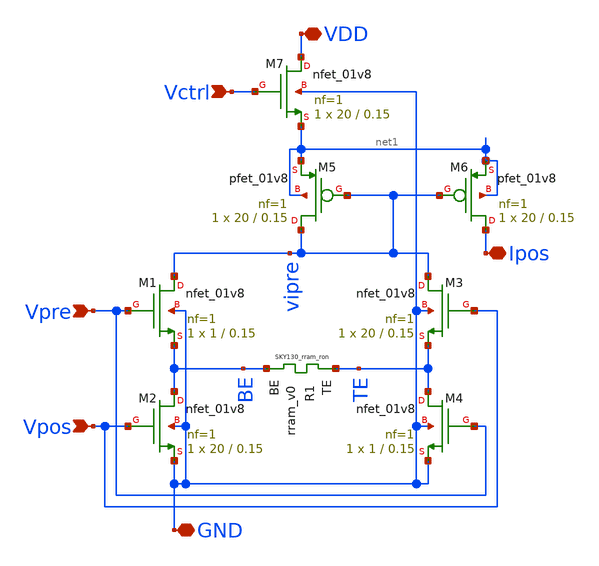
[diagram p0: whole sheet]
** sch_path: synapse/7T1R.sch
**.subckt 7T1R Vpre Vpos GND Ipos VDD Vctrl
*.ipin Vpre
*.ipin Vpos
*.iopin GND
*.iopin Ipos
*.iopin VDD
*.ipin Vctrl
XM1 vipre Vpre BE GND sky130_fd_pr__nfet_01v8 L=0.15 W=1 nf=1 ad='int((nf+1)/2) * W/nf * 0.29' as='int((nf+2)/2) * W/nf * 0.29'
+ pd='2*int((nf+1)/2) * (W/nf + 0.29)' ps='2*int((nf+2)/2) * (W/nf + 0.29)' nrd='0.29 / W' nrs='0.29 / W'
+ sa=0 sb=0 sd=0 mult=1 m=1
XR1 TE BE rram_v0
XM3 vipre Vpos TE GND sky130_fd_pr__nfet_01v8 L=0.15 W=20 nf=1 ad='int((nf+1)/2) * W/nf * 0.29' as='int((nf+2)/2) * W/nf * 0.29'
+ pd='2*int((nf+1)/2) * (W/nf + 0.29)' ps='2*int((nf+2)/2) * (W/nf + 0.29)' nrd='0.29 / W' nrs='0.29 / W'
+ sa=0 sb=0 sd=0 mult=1 m=1
XM6 Ipos vipre net1 net1 sky130_fd_pr__pfet_01v8 L=0.15 W=20 nf=1 ad='int((nf+1)/2) * W/nf * 0.29' as='int((nf+2)/2) * W/nf * 0.29'
+ pd='2*int((nf+1)/2) * (W/nf + 0.29)' ps='2*int((nf+2)/2) * (W/nf + 0.29)' nrd='0.29 / W' nrs='0.29 / W'
+ sa=0 sb=0 sd=0 mult=1 m=1
XM5 vipre vipre net1 net1 sky130_fd_pr__pfet_01v8 L=0.15 W=20 nf=1 ad='int((nf+1)/2) * W/nf * 0.29' as='int((nf+2)/2) * W/nf * 0.29'
+ pd='2*int((nf+1)/2) * (W/nf + 0.29)' ps='2*int((nf+2)/2) * (W/nf + 0.29)' nrd='0.29 / W' nrs='0.29 / W'
+ sa=0 sb=0 sd=0 mult=1 m=1
XM2 BE Vpos GND GND sky130_fd_pr__nfet_01v8 L=0.15 W=20 nf=1 ad='int((nf+1)/2) * W/nf * 0.29' as='int((nf+2)/2) * W/nf * 0.29'
+ pd='2*int((nf+1)/2) * (W/nf + 0.29)' ps='2*int((nf+2)/2) * (W/nf + 0.29)' nrd='0.29 / W' nrs='0.29 / W'
+ sa=0 sb=0 sd=0 mult=1 m=1
XM4 TE Vpre GND GND sky130_fd_pr__nfet_01v8 L=0.15 W=1 nf=1 ad='int((nf+1)/2) * W/nf * 0.29' as='int((nf+2)/2) * W/nf * 0.29'
+ pd='2*int((nf+1)/2) * (W/nf + 0.29)' ps='2*int((nf+2)/2) * (W/nf + 0.29)' nrd='0.29 / W' nrs='0.29 / W'
+ sa=0 sb=0 sd=0 mult=1 m=1
XM7 VDD Vctrl net1 GND sky130_fd_pr__nfet_01v8 L=0.15 W=20 nf=1 ad='int((nf+1)/2) * W/nf * 0.29' as='int((nf+2)/2) * W/nf * 0.29'
+ pd='2*int((nf+1)/2) * (W/nf + 0.29)' ps='2*int((nf+2)/2) * (W/nf + 0.29)' nrd='0.29 / W' nrs='0.29 / W'
+ sa=0 sb=0 sd=0 mult=1 m=1
**.ends
.end
